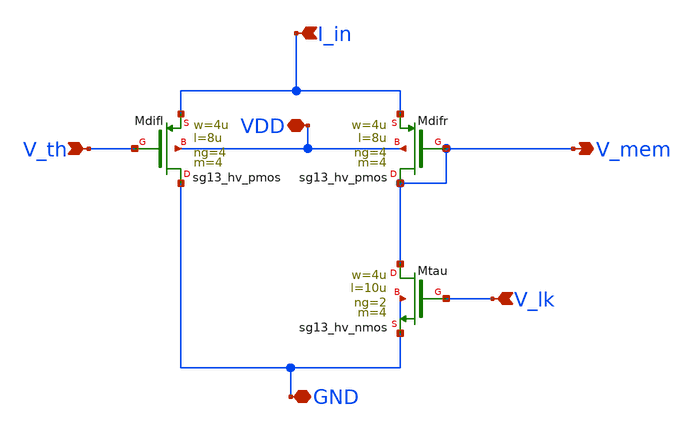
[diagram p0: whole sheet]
** sch_path: xschem/DPI.sch
**.subckt DPI V_mem V_lk V_th I_in VDD GND
*.opin V_mem
*.ipin V_lk
*.ipin V_th
*.ipin I_in
*.iopin VDD
*.iopin GND
XMdifl GND V_th I_in VDD sg13_hv_pmos w=4u l=8u ng=4 m=4 mm_ok=1
XMdifr V_mem V_mem I_in VDD sg13_hv_pmos w=4u l=8u ng=4 m=4 mm_ok=1
XMtau V_mem V_lk GND GND sg13_hv_nmos w=4u l=10u ng=2 m=4 mm_ok=1
**.ends
.end
